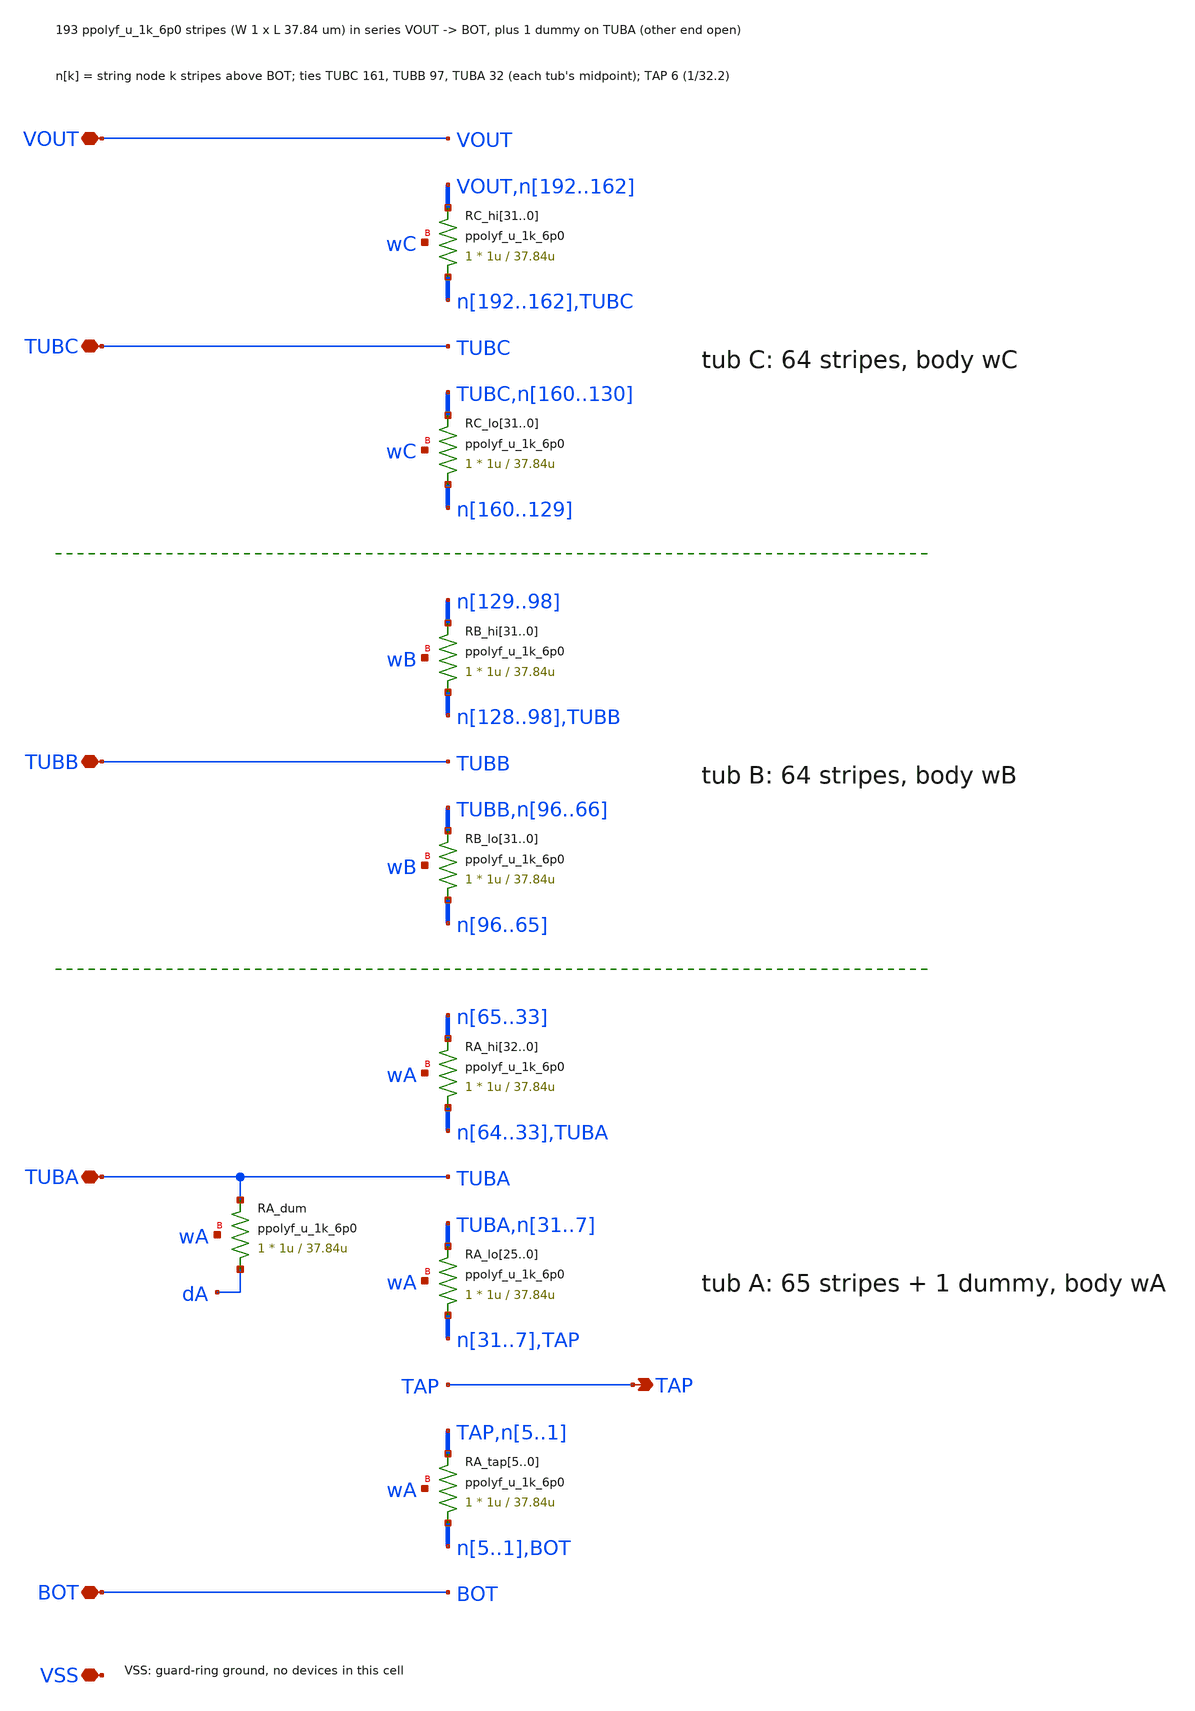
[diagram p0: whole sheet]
** sch_path: xschem/divider.sch
**.subckt divider VOUT TUBC TUBB TUBA TAP BOT VSS
*.iopin VOUT
*.iopin TUBC
*.iopin TUBB
*.iopin TUBA
*.opin TAP
*.iopin BOT
*.iopin VSS
XRC_hi31 n192 VOUT wC ppolyf_u_1k_6p0 r_width=1u r_length=37.84u m=1
XRC_hi30 n191 n192 wC ppolyf_u_1k_6p0 r_width=1u r_length=37.84u m=1
XRC_hi29 n190 n191 wC ppolyf_u_1k_6p0 r_width=1u r_length=37.84u m=1
XRC_hi28 n189 n190 wC ppolyf_u_1k_6p0 r_width=1u r_length=37.84u m=1
XRC_hi27 n188 n189 wC ppolyf_u_1k_6p0 r_width=1u r_length=37.84u m=1
XRC_hi26 n187 n188 wC ppolyf_u_1k_6p0 r_width=1u r_length=37.84u m=1
XRC_hi25 n186 n187 wC ppolyf_u_1k_6p0 r_width=1u r_length=37.84u m=1
XRC_hi24 n185 n186 wC ppolyf_u_1k_6p0 r_width=1u r_length=37.84u m=1
XRC_hi23 n184 n185 wC ppolyf_u_1k_6p0 r_width=1u r_length=37.84u m=1
XRC_hi22 n183 n184 wC ppolyf_u_1k_6p0 r_width=1u r_length=37.84u m=1
XRC_hi21 n182 n183 wC ppolyf_u_1k_6p0 r_width=1u r_length=37.84u m=1
XRC_hi20 n181 n182 wC ppolyf_u_1k_6p0 r_width=1u r_length=37.84u m=1
XRC_hi19 n180 n181 wC ppolyf_u_1k_6p0 r_width=1u r_length=37.84u m=1
XRC_hi18 n179 n180 wC ppolyf_u_1k_6p0 r_width=1u r_length=37.84u m=1
XRC_hi17 n178 n179 wC ppolyf_u_1k_6p0 r_width=1u r_length=37.84u m=1
XRC_hi16 n177 n178 wC ppolyf_u_1k_6p0 r_width=1u r_length=37.84u m=1
XRC_hi15 n176 n177 wC ppolyf_u_1k_6p0 r_width=1u r_length=37.84u m=1
XRC_hi14 n175 n176 wC ppolyf_u_1k_6p0 r_width=1u r_length=37.84u m=1
XRC_hi13 n174 n175 wC ppolyf_u_1k_6p0 r_width=1u r_length=37.84u m=1
XRC_hi12 n173 n174 wC ppolyf_u_1k_6p0 r_width=1u r_length=37.84u m=1
XRC_hi11 n172 n173 wC ppolyf_u_1k_6p0 r_width=1u r_length=37.84u m=1
XRC_hi10 n171 n172 wC ppolyf_u_1k_6p0 r_width=1u r_length=37.84u m=1
XRC_hi9 n170 n171 wC ppolyf_u_1k_6p0 r_width=1u r_length=37.84u m=1
XRC_hi8 n169 n170 wC ppolyf_u_1k_6p0 r_width=1u r_length=37.84u m=1
XRC_hi7 n168 n169 wC ppolyf_u_1k_6p0 r_width=1u r_length=37.84u m=1
XRC_hi6 n167 n168 wC ppolyf_u_1k_6p0 r_width=1u r_length=37.84u m=1
XRC_hi5 n166 n167 wC ppolyf_u_1k_6p0 r_width=1u r_length=37.84u m=1
XRC_hi4 n165 n166 wC ppolyf_u_1k_6p0 r_width=1u r_length=37.84u m=1
XRC_hi3 n164 n165 wC ppolyf_u_1k_6p0 r_width=1u r_length=37.84u m=1
XRC_hi2 n163 n164 wC ppolyf_u_1k_6p0 r_width=1u r_length=37.84u m=1
XRC_hi1 n162 n163 wC ppolyf_u_1k_6p0 r_width=1u r_length=37.84u m=1
XRC_hi0 TUBC n162 wC ppolyf_u_1k_6p0 r_width=1u r_length=37.84u m=1
XRC_lo31 n160 TUBC wC ppolyf_u_1k_6p0 r_width=1u r_length=37.84u m=1
XRC_lo30 n159 n160 wC ppolyf_u_1k_6p0 r_width=1u r_length=37.84u m=1
XRC_lo29 n158 n159 wC ppolyf_u_1k_6p0 r_width=1u r_length=37.84u m=1
XRC_lo28 n157 n158 wC ppolyf_u_1k_6p0 r_width=1u r_length=37.84u m=1
XRC_lo27 n156 n157 wC ppolyf_u_1k_6p0 r_width=1u r_length=37.84u m=1
XRC_lo26 n155 n156 wC ppolyf_u_1k_6p0 r_width=1u r_length=37.84u m=1
XRC_lo25 n154 n155 wC ppolyf_u_1k_6p0 r_width=1u r_length=37.84u m=1
XRC_lo24 n153 n154 wC ppolyf_u_1k_6p0 r_width=1u r_length=37.84u m=1
XRC_lo23 n152 n153 wC ppolyf_u_1k_6p0 r_width=1u r_length=37.84u m=1
XRC_lo22 n151 n152 wC ppolyf_u_1k_6p0 r_width=1u r_length=37.84u m=1
XRC_lo21 n150 n151 wC ppolyf_u_1k_6p0 r_width=1u r_length=37.84u m=1
XRC_lo20 n149 n150 wC ppolyf_u_1k_6p0 r_width=1u r_length=37.84u m=1
XRC_lo19 n148 n149 wC ppolyf_u_1k_6p0 r_width=1u r_length=37.84u m=1
XRC_lo18 n147 n148 wC ppolyf_u_1k_6p0 r_width=1u r_length=37.84u m=1
XRC_lo17 n146 n147 wC ppolyf_u_1k_6p0 r_width=1u r_length=37.84u m=1
XRC_lo16 n145 n146 wC ppolyf_u_1k_6p0 r_width=1u r_length=37.84u m=1
XRC_lo15 n144 n145 wC ppolyf_u_1k_6p0 r_width=1u r_length=37.84u m=1
XRC_lo14 n143 n144 wC ppolyf_u_1k_6p0 r_width=1u r_length=37.84u m=1
XRC_lo13 n142 n143 wC ppolyf_u_1k_6p0 r_width=1u r_length=37.84u m=1
XRC_lo12 n141 n142 wC ppolyf_u_1k_6p0 r_width=1u r_length=37.84u m=1
XRC_lo11 n140 n141 wC ppolyf_u_1k_6p0 r_width=1u r_length=37.84u m=1
XRC_lo10 n139 n140 wC ppolyf_u_1k_6p0 r_width=1u r_length=37.84u m=1
XRC_lo9 n138 n139 wC ppolyf_u_1k_6p0 r_width=1u r_length=37.84u m=1
XRC_lo8 n137 n138 wC ppolyf_u_1k_6p0 r_width=1u r_length=37.84u m=1
XRC_lo7 n136 n137 wC ppolyf_u_1k_6p0 r_width=1u r_length=37.84u m=1
XRC_lo6 n135 n136 wC ppolyf_u_1k_6p0 r_width=1u r_length=37.84u m=1
XRC_lo5 n134 n135 wC ppolyf_u_1k_6p0 r_width=1u r_length=37.84u m=1
XRC_lo4 n133 n134 wC ppolyf_u_1k_6p0 r_width=1u r_length=37.84u m=1
XRC_lo3 n132 n133 wC ppolyf_u_1k_6p0 r_width=1u r_length=37.84u m=1
XRC_lo2 n131 n132 wC ppolyf_u_1k_6p0 r_width=1u r_length=37.84u m=1
XRC_lo1 n130 n131 wC ppolyf_u_1k_6p0 r_width=1u r_length=37.84u m=1
XRC_lo0 n129 n130 wC ppolyf_u_1k_6p0 r_width=1u r_length=37.84u m=1
XRB_hi31 n128 n129 wB ppolyf_u_1k_6p0 r_width=1u r_length=37.84u m=1
XRB_hi30 n127 n128 wB ppolyf_u_1k_6p0 r_width=1u r_length=37.84u m=1
XRB_hi29 n126 n127 wB ppolyf_u_1k_6p0 r_width=1u r_length=37.84u m=1
XRB_hi28 n125 n126 wB ppolyf_u_1k_6p0 r_width=1u r_length=37.84u m=1
XRB_hi27 n124 n125 wB ppolyf_u_1k_6p0 r_width=1u r_length=37.84u m=1
XRB_hi26 n123 n124 wB ppolyf_u_1k_6p0 r_width=1u r_length=37.84u m=1
XRB_hi25 n122 n123 wB ppolyf_u_1k_6p0 r_width=1u r_length=37.84u m=1
XRB_hi24 n121 n122 wB ppolyf_u_1k_6p0 r_width=1u r_length=37.84u m=1
XRB_hi23 n120 n121 wB ppolyf_u_1k_6p0 r_width=1u r_length=37.84u m=1
XRB_hi22 n119 n120 wB ppolyf_u_1k_6p0 r_width=1u r_length=37.84u m=1
XRB_hi21 n118 n119 wB ppolyf_u_1k_6p0 r_width=1u r_length=37.84u m=1
XRB_hi20 n117 n118 wB ppolyf_u_1k_6p0 r_width=1u r_length=37.84u m=1
XRB_hi19 n116 n117 wB ppolyf_u_1k_6p0 r_width=1u r_length=37.84u m=1
XRB_hi18 n115 n116 wB ppolyf_u_1k_6p0 r_width=1u r_length=37.84u m=1
XRB_hi17 n114 n115 wB ppolyf_u_1k_6p0 r_width=1u r_length=37.84u m=1
XRB_hi16 n113 n114 wB ppolyf_u_1k_6p0 r_width=1u r_length=37.84u m=1
XRB_hi15 n112 n113 wB ppolyf_u_1k_6p0 r_width=1u r_length=37.84u m=1
XRB_hi14 n111 n112 wB ppolyf_u_1k_6p0 r_width=1u r_length=37.84u m=1
XRB_hi13 n110 n111 wB ppolyf_u_1k_6p0 r_width=1u r_length=37.84u m=1
XRB_hi12 n109 n110 wB ppolyf_u_1k_6p0 r_width=1u r_length=37.84u m=1
XRB_hi11 n108 n109 wB ppolyf_u_1k_6p0 r_width=1u r_length=37.84u m=1
XRB_hi10 n107 n108 wB ppolyf_u_1k_6p0 r_width=1u r_length=37.84u m=1
XRB_hi9 n106 n107 wB ppolyf_u_1k_6p0 r_width=1u r_length=37.84u m=1
XRB_hi8 n105 n106 wB ppolyf_u_1k_6p0 r_width=1u r_length=37.84u m=1
XRB_hi7 n104 n105 wB ppolyf_u_1k_6p0 r_width=1u r_length=37.84u m=1
XRB_hi6 n103 n104 wB ppolyf_u_1k_6p0 r_width=1u r_length=37.84u m=1
XRB_hi5 n102 n103 wB ppolyf_u_1k_6p0 r_width=1u r_length=37.84u m=1
XRB_hi4 n101 n102 wB ppolyf_u_1k_6p0 r_width=1u r_length=37.84u m=1
XRB_hi3 n100 n101 wB ppolyf_u_1k_6p0 r_width=1u r_length=37.84u m=1
XRB_hi2 n99 n100 wB ppolyf_u_1k_6p0 r_width=1u r_length=37.84u m=1
XRB_hi1 n98 n99 wB ppolyf_u_1k_6p0 r_width=1u r_length=37.84u m=1
XRB_hi0 TUBB n98 wB ppolyf_u_1k_6p0 r_width=1u r_length=37.84u m=1
XRB_lo31 n96 TUBB wB ppolyf_u_1k_6p0 r_width=1u r_length=37.84u m=1
XRB_lo30 n95 n96 wB ppolyf_u_1k_6p0 r_width=1u r_length=37.84u m=1
XRB_lo29 n94 n95 wB ppolyf_u_1k_6p0 r_width=1u r_length=37.84u m=1
XRB_lo28 n93 n94 wB ppolyf_u_1k_6p0 r_width=1u r_length=37.84u m=1
XRB_lo27 n92 n93 wB ppolyf_u_1k_6p0 r_width=1u r_length=37.84u m=1
XRB_lo26 n91 n92 wB ppolyf_u_1k_6p0 r_width=1u r_length=37.84u m=1
XRB_lo25 n90 n91 wB ppolyf_u_1k_6p0 r_width=1u r_length=37.84u m=1
XRB_lo24 n89 n90 wB ppolyf_u_1k_6p0 r_width=1u r_length=37.84u m=1
XRB_lo23 n88 n89 wB ppolyf_u_1k_6p0 r_width=1u r_length=37.84u m=1
XRB_lo22 n87 n88 wB ppolyf_u_1k_6p0 r_width=1u r_length=37.84u m=1
XRB_lo21 n86 n87 wB ppolyf_u_1k_6p0 r_width=1u r_length=37.84u m=1
XRB_lo20 n85 n86 wB ppolyf_u_1k_6p0 r_width=1u r_length=37.84u m=1
XRB_lo19 n84 n85 wB ppolyf_u_1k_6p0 r_width=1u r_length=37.84u m=1
XRB_lo18 n83 n84 wB ppolyf_u_1k_6p0 r_width=1u r_length=37.84u m=1
XRB_lo17 n82 n83 wB ppolyf_u_1k_6p0 r_width=1u r_length=37.84u m=1
XRB_lo16 n81 n82 wB ppolyf_u_1k_6p0 r_width=1u r_length=37.84u m=1
XRB_lo15 n80 n81 wB ppolyf_u_1k_6p0 r_width=1u r_length=37.84u m=1
XRB_lo14 n79 n80 wB ppolyf_u_1k_6p0 r_width=1u r_length=37.84u m=1
XRB_lo13 n78 n79 wB ppolyf_u_1k_6p0 r_width=1u r_length=37.84u m=1
XRB_lo12 n77 n78 wB ppolyf_u_1k_6p0 r_width=1u r_length=37.84u m=1
XRB_lo11 n76 n77 wB ppolyf_u_1k_6p0 r_width=1u r_length=37.84u m=1
XRB_lo10 n75 n76 wB ppolyf_u_1k_6p0 r_width=1u r_length=37.84u m=1
XRB_lo9 n74 n75 wB ppolyf_u_1k_6p0 r_width=1u r_length=37.84u m=1
XRB_lo8 n73 n74 wB ppolyf_u_1k_6p0 r_width=1u r_length=37.84u m=1
XRB_lo7 n72 n73 wB ppolyf_u_1k_6p0 r_width=1u r_length=37.84u m=1
XRB_lo6 n71 n72 wB ppolyf_u_1k_6p0 r_width=1u r_length=37.84u m=1
XRB_lo5 n70 n71 wB ppolyf_u_1k_6p0 r_width=1u r_length=37.84u m=1
XRB_lo4 n69 n70 wB ppolyf_u_1k_6p0 r_width=1u r_length=37.84u m=1
XRB_lo3 n68 n69 wB ppolyf_u_1k_6p0 r_width=1u r_length=37.84u m=1
XRB_lo2 n67 n68 wB ppolyf_u_1k_6p0 r_width=1u r_length=37.84u m=1
XRB_lo1 n66 n67 wB ppolyf_u_1k_6p0 r_width=1u r_length=37.84u m=1
XRB_lo0 n65 n66 wB ppolyf_u_1k_6p0 r_width=1u r_length=37.84u m=1
XRA_hi32 n64 n65 wA ppolyf_u_1k_6p0 r_width=1u r_length=37.84u m=1
XRA_hi31 n63 n64 wA ppolyf_u_1k_6p0 r_width=1u r_length=37.84u m=1
XRA_hi30 n62 n63 wA ppolyf_u_1k_6p0 r_width=1u r_length=37.84u m=1
XRA_hi29 n61 n62 wA ppolyf_u_1k_6p0 r_width=1u r_length=37.84u m=1
XRA_hi28 n60 n61 wA ppolyf_u_1k_6p0 r_width=1u r_length=37.84u m=1
XRA_hi27 n59 n60 wA ppolyf_u_1k_6p0 r_width=1u r_length=37.84u m=1
XRA_hi26 n58 n59 wA ppolyf_u_1k_6p0 r_width=1u r_length=37.84u m=1
XRA_hi25 n57 n58 wA ppolyf_u_1k_6p0 r_width=1u r_length=37.84u m=1
XRA_hi24 n56 n57 wA ppolyf_u_1k_6p0 r_width=1u r_length=37.84u m=1
XRA_hi23 n55 n56 wA ppolyf_u_1k_6p0 r_width=1u r_length=37.84u m=1
XRA_hi22 n54 n55 wA ppolyf_u_1k_6p0 r_width=1u r_length=37.84u m=1
XRA_hi21 n53 n54 wA ppolyf_u_1k_6p0 r_width=1u r_length=37.84u m=1
XRA_hi20 n52 n53 wA ppolyf_u_1k_6p0 r_width=1u r_length=37.84u m=1
XRA_hi19 n51 n52 wA ppolyf_u_1k_6p0 r_width=1u r_length=37.84u m=1
XRA_hi18 n50 n51 wA ppolyf_u_1k_6p0 r_width=1u r_length=37.84u m=1
XRA_hi17 n49 n50 wA ppolyf_u_1k_6p0 r_width=1u r_length=37.84u m=1
XRA_hi16 n48 n49 wA ppolyf_u_1k_6p0 r_width=1u r_length=37.84u m=1
XRA_hi15 n47 n48 wA ppolyf_u_1k_6p0 r_width=1u r_length=37.84u m=1
XRA_hi14 n46 n47 wA ppolyf_u_1k_6p0 r_width=1u r_length=37.84u m=1
XRA_hi13 n45 n46 wA ppolyf_u_1k_6p0 r_width=1u r_length=37.84u m=1
XRA_hi12 n44 n45 wA ppolyf_u_1k_6p0 r_width=1u r_length=37.84u m=1
XRA_hi11 n43 n44 wA ppolyf_u_1k_6p0 r_width=1u r_length=37.84u m=1
XRA_hi10 n42 n43 wA ppolyf_u_1k_6p0 r_width=1u r_length=37.84u m=1
XRA_hi9 n41 n42 wA ppolyf_u_1k_6p0 r_width=1u r_length=37.84u m=1
XRA_hi8 n40 n41 wA ppolyf_u_1k_6p0 r_width=1u r_length=37.84u m=1
XRA_hi7 n39 n40 wA ppolyf_u_1k_6p0 r_width=1u r_length=37.84u m=1
XRA_hi6 n38 n39 wA ppolyf_u_1k_6p0 r_width=1u r_length=37.84u m=1
XRA_hi5 n37 n38 wA ppolyf_u_1k_6p0 r_width=1u r_length=37.84u m=1
XRA_hi4 n36 n37 wA ppolyf_u_1k_6p0 r_width=1u r_length=37.84u m=1
XRA_hi3 n35 n36 wA ppolyf_u_1k_6p0 r_width=1u r_length=37.84u m=1
XRA_hi2 n34 n35 wA ppolyf_u_1k_6p0 r_width=1u r_length=37.84u m=1
XRA_hi1 n33 n34 wA ppolyf_u_1k_6p0 r_width=1u r_length=37.84u m=1
XRA_hi0 TUBA n33 wA ppolyf_u_1k_6p0 r_width=1u r_length=37.84u m=1
XRA_lo25 n31 TUBA wA ppolyf_u_1k_6p0 r_width=1u r_length=37.84u m=1
XRA_lo24 n30 n31 wA ppolyf_u_1k_6p0 r_width=1u r_length=37.84u m=1
XRA_lo23 n29 n30 wA ppolyf_u_1k_6p0 r_width=1u r_length=37.84u m=1
XRA_lo22 n28 n29 wA ppolyf_u_1k_6p0 r_width=1u r_length=37.84u m=1
XRA_lo21 n27 n28 wA ppolyf_u_1k_6p0 r_width=1u r_length=37.84u m=1
XRA_lo20 n26 n27 wA ppolyf_u_1k_6p0 r_width=1u r_length=37.84u m=1
XRA_lo19 n25 n26 wA ppolyf_u_1k_6p0 r_width=1u r_length=37.84u m=1
XRA_lo18 n24 n25 wA ppolyf_u_1k_6p0 r_width=1u r_length=37.84u m=1
XRA_lo17 n23 n24 wA ppolyf_u_1k_6p0 r_width=1u r_length=37.84u m=1
XRA_lo16 n22 n23 wA ppolyf_u_1k_6p0 r_width=1u r_length=37.84u m=1
XRA_lo15 n21 n22 wA ppolyf_u_1k_6p0 r_width=1u r_length=37.84u m=1
XRA_lo14 n20 n21 wA ppolyf_u_1k_6p0 r_width=1u r_length=37.84u m=1
XRA_lo13 n19 n20 wA ppolyf_u_1k_6p0 r_width=1u r_length=37.84u m=1
XRA_lo12 n18 n19 wA ppolyf_u_1k_6p0 r_width=1u r_length=37.84u m=1
XRA_lo11 n17 n18 wA ppolyf_u_1k_6p0 r_width=1u r_length=37.84u m=1
XRA_lo10 n16 n17 wA ppolyf_u_1k_6p0 r_width=1u r_length=37.84u m=1
XRA_lo9 n15 n16 wA ppolyf_u_1k_6p0 r_width=1u r_length=37.84u m=1
XRA_lo8 n14 n15 wA ppolyf_u_1k_6p0 r_width=1u r_length=37.84u m=1
XRA_lo7 n13 n14 wA ppolyf_u_1k_6p0 r_width=1u r_length=37.84u m=1
XRA_lo6 n12 n13 wA ppolyf_u_1k_6p0 r_width=1u r_length=37.84u m=1
XRA_lo5 n11 n12 wA ppolyf_u_1k_6p0 r_width=1u r_length=37.84u m=1
XRA_lo4 n10 n11 wA ppolyf_u_1k_6p0 r_width=1u r_length=37.84u m=1
XRA_lo3 n9 n10 wA ppolyf_u_1k_6p0 r_width=1u r_length=37.84u m=1
XRA_lo2 n8 n9 wA ppolyf_u_1k_6p0 r_width=1u r_length=37.84u m=1
XRA_lo1 n7 n8 wA ppolyf_u_1k_6p0 r_width=1u r_length=37.84u m=1
XRA_lo0 TAP n7 wA ppolyf_u_1k_6p0 r_width=1u r_length=37.84u m=1
XRA_tap5 n5 TAP wA ppolyf_u_1k_6p0 r_width=1u r_length=37.84u m=1
XRA_tap4 n4 n5 wA ppolyf_u_1k_6p0 r_width=1u r_length=37.84u m=1
XRA_tap3 n3 n4 wA ppolyf_u_1k_6p0 r_width=1u r_length=37.84u m=1
XRA_tap2 n2 n3 wA ppolyf_u_1k_6p0 r_width=1u r_length=37.84u m=1
XRA_tap1 n1 n2 wA ppolyf_u_1k_6p0 r_width=1u r_length=37.84u m=1
XRA_tap0 BOT n1 wA ppolyf_u_1k_6p0 r_width=1u r_length=37.84u m=1
XRA_dum dA TUBA wA ppolyf_u_1k_6p0 r_width=1u r_length=37.84u m=1
**.ends
.end
